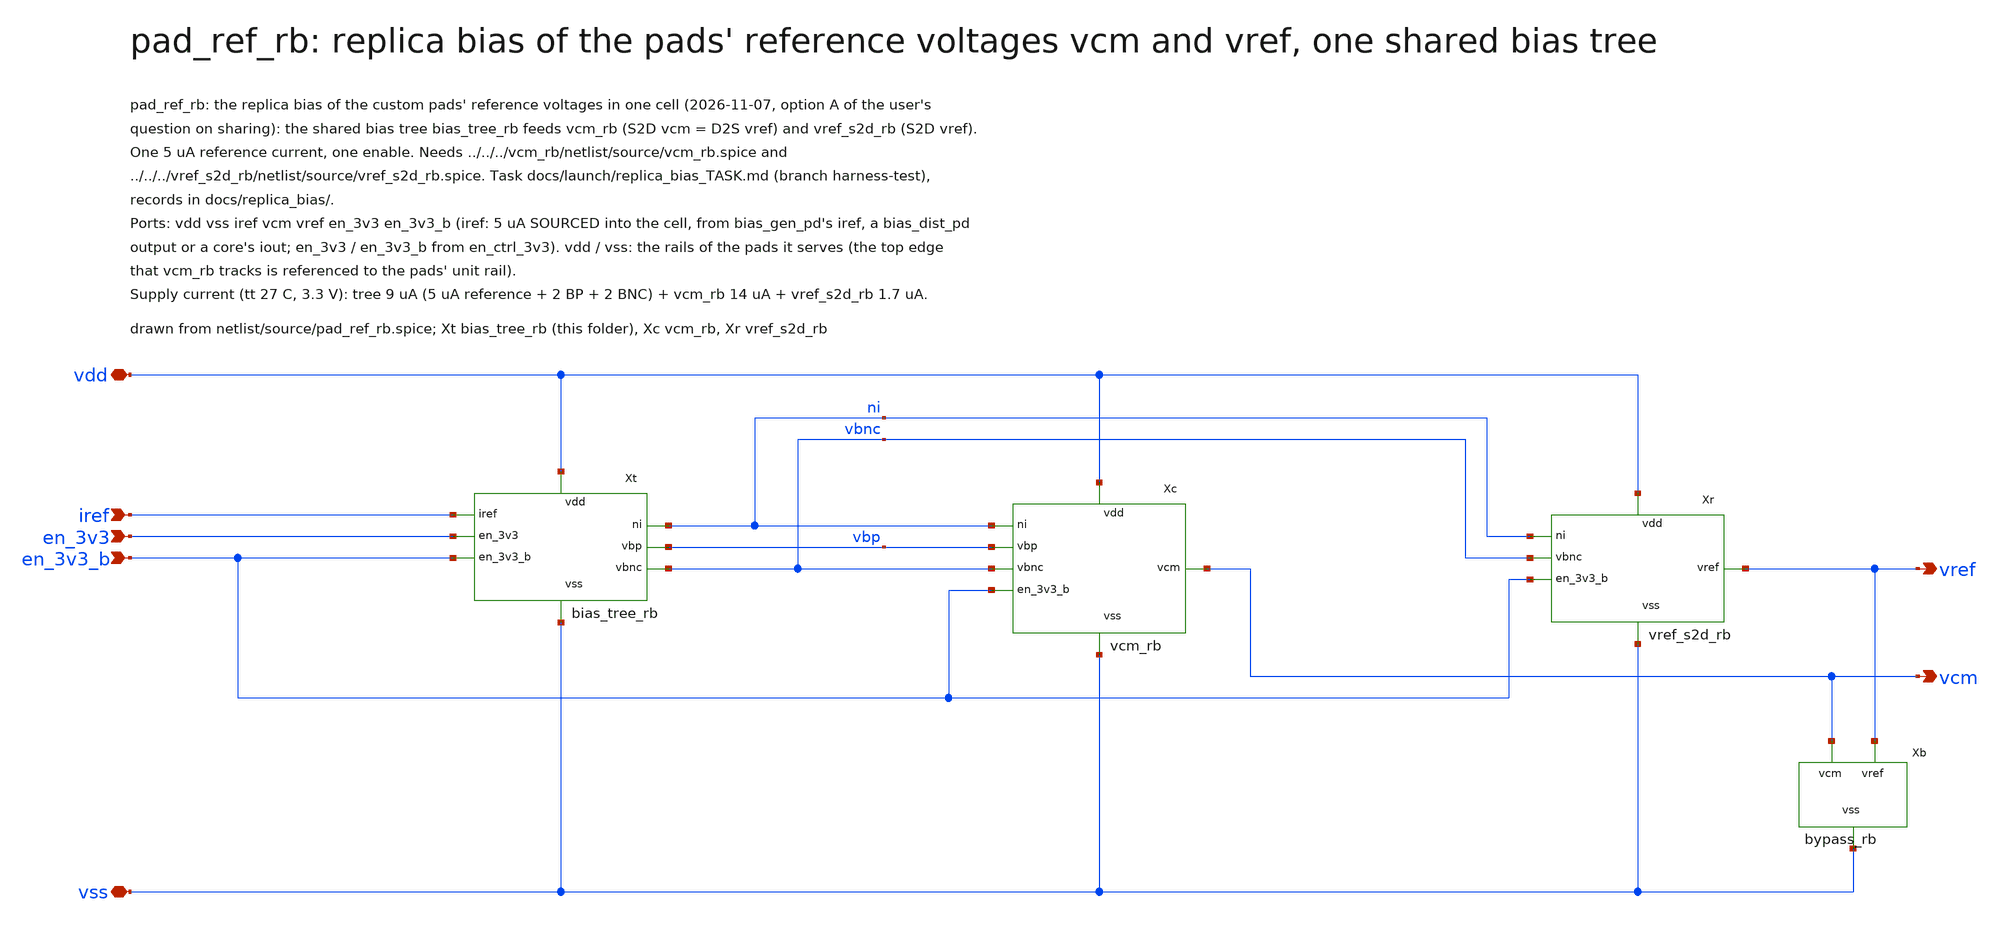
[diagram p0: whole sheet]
** sch_path: macros/pad_ref_rb/schematic/xschem/pad_ref_rb.sch
**.subckt pad_ref_rb vdd vss iref vcm vref en_3v3 en_3v3_b
*.iopin vdd
*.iopin vss
*.ipin iref
*.opin vcm
*.opin vref
*.ipin en_3v3
*.ipin en_3v3_b
Xt vdd vss iref ni vbp vbnc en_3v3 en_3v3_b bias_tree_rb
Xc vdd vss ni vbp vbnc vcm en_3v3_b vcm_rb
Xr vdd vss ni vbnc vref en_3v3_b vref_s2d_rb
Xb vss vcm vref bypass_rb
**.ends

* expanding   symbol:  bias_tree_rb.sym # of pins=8
** sym_path: macros/pad_ref_rb/schematic/xschem/bias_tree_rb.sym
** sch_path: macros/pad_ref_rb/schematic/xschem/bias_tree_rb.sch
.subckt bias_tree_rb vdd vss iref ni vbp vbnc en_3v3 en_3v3_b
*.iopin vdd
*.iopin vss
*.ipin iref
*.opin ni
*.opin vbp
*.opin vbnc
*.ipin en_3v3
*.ipin en_3v3_b
XTGN iref en_3v3 ni vss sg13_hv_nmos w=1u l=0.45u ng=1 m=1 mm_ok=1
XTGP ni en_3v3_b iref vdd sg13_hv_pmos w=1u l=0.45u ng=1 m=1 mm_ok=1
XTDN ni en_3v3_b vss vss sg13_hv_nmos w=1u l=0.45u ng=1 m=1 mm_ok=1
XNI ni ni vss vss sg13_hv_nmos w=6u l=6u ng=1 m=1 mm_ok=1
XNBP vbp ni vss vss sg13_hv_nmos w=2.4u l=6u ng=1 m=1 mm_ok=1
XBP vbp vbp vdd vdd sg13_hv_pmos w=2u l=6u ng=1 m=1 mm_ok=1
XPBNC vbnc vbp vdd vdd sg13_hv_pmos w=2u l=6u ng=1 m=1 mm_ok=1
XBNC vbnc vbnc vss vss sg13_hv_nmos w=1u l=8u ng=1 m=1 mm_ok=1
XMDPBN vdd vbp vdd vdd sg13_hv_pmos w=5u l=6u ng=1 m=1 mm_ok=1
.ends


* expanding   symbol:  vcm_rb.sym # of pins=7
** sym_path: macros/vcm_rb/schematic/xschem/vcm_rb.sym
** sch_path: macros/vcm_rb/schematic/xschem/vcm_rb.sch
.subckt vcm_rb vdd vss ni vbp vbnc vcm en_3v3_b
*.iopin vdd
*.iopin vss
*.ipin ni
*.ipin vbp
*.ipin vbnc
*.opin vcm
*.ipin en_3v3_b
XTR ts vbp vdd vdd sg13_hv_pmos w=5u l=6u ng=1 m=1 mm_ok=1
XMR gh gh ts ts sg13_hv_pmos w=20u l=1u ng=2 m=1 mm_ok=1
XSH1 gh ni vss vss sg13_hv_nmos w=2.4u l=6u ng=1 m=1 mm_ok=1
XSH2 gh ni vss vss sg13_hv_nmos w=2.4u l=6u ng=1 m=1 mm_ok=1
XCY vdd vbnc xp vss sg13_hv_nmos w=15u l=3u ng=1 m=1 mm_ok=1
XSY xp ni vss vss sg13_hv_nmos w=6u l=6u ng=1 m=1 mm_ok=1
XSU m m gh gh sg13_hv_pmos w=1u l=4u ng=1 m=1 mm_ok=1
XSL1 xp xp m m sg13_hv_pmos w=1u l=4u ng=1 m=1 mm_ok=1
XSL2 xp xp m m sg13_hv_pmos w=1u l=4u ng=1 m=1 mm_ok=1
XBT bt vbp vdd vdd sg13_hv_pmos w=5u l=6u ng=1 m=1 mm_ok=1
XBA bd m bt bt sg13_hv_pmos w=20u l=1u ng=2 m=1 mm_ok=1
XBB vcm vcm bt bt sg13_hv_pmos w=20u l=1u ng=2 m=1 mm_ok=1
XBD bd bd vss vss sg13_hv_nmos w=6u l=6u ng=1 m=1 mm_ok=1
XBM vcm bd vss vss sg13_hv_nmos w=6u l=6u ng=1 m=1 mm_ok=1
XCB vss vcm vss vss sg13_hv_nmos w=12u l=12u ng=1 m=1 mm_ok=1
XSPD vcm en_3v3_b vss vss sg13_hv_nmos w=1u l=0.45u ng=1 m=1 mm_ok=1
XMDT[1] vdd vbp vdd vdd sg13_hv_pmos w=5u l=6u ng=1 m=1 mm_ok=1
XMDT[0] vdd vbp vdd vdd sg13_hv_pmos w=5u l=6u ng=1 m=1 mm_ok=1
XMDU[1] vdd vdd vdd vdd sg13_hv_pmos w=20u l=1u ng=2 m=1 mm_ok=1
XMDU[0] vdd vdd vdd vdd sg13_hv_pmos w=20u l=1u ng=2 m=1 mm_ok=1
XMDAU[1] gh m gh gh sg13_hv_pmos w=1u l=4u ng=1 m=1 mm_ok=1
XMDAU[0] gh m gh gh sg13_hv_pmos w=1u l=4u ng=1 m=1 mm_ok=1
XMDAL[1] m xp m m sg13_hv_pmos w=1u l=4u ng=1 m=1 mm_ok=1
XMDAL[0] m xp m m sg13_hv_pmos w=1u l=4u ng=1 m=1 mm_ok=1
XMDM[1] vss bd vss vss sg13_hv_nmos w=2u l=6u ng=1 m=1 mm_ok=1
XMDM[0] vss bd vss vss sg13_hv_nmos w=2u l=6u ng=1 m=1 mm_ok=1
.ends


* expanding   symbol:  vref_s2d_rb.sym # of pins=6
** sym_path: macros/vref_s2d_rb/schematic/xschem/vref_s2d_rb.sym
** sch_path: macros/vref_s2d_rb/schematic/xschem/vref_s2d_rb.sch
.subckt vref_s2d_rb vdd vss ni vbnc vref en_3v3_b
*.iopin vdd
*.iopin vss
*.ipin ni
*.ipin vbnc
*.opin vref
*.ipin en_3v3_b
XF1 vdd vbnc vref vss sg13_hv_nmos w=15u l=3u ng=1 m=1 mm_ok=1
XF2 vdd vbnc vref vss sg13_hv_nmos w=15u l=3u ng=1 m=1 mm_ok=1
XF3 vdd vbnc vref vss sg13_hv_nmos w=15u l=3u ng=1 m=1 mm_ok=1
XF4 vdd vbnc vref vss sg13_hv_nmos w=15u l=3u ng=1 m=1 mm_ok=1
XSF vref ni vss vss sg13_hv_nmos w=2u l=6u ng=1 m=1 mm_ok=1
XCB1 vss vref vss vss sg13_hv_nmos w=12u l=12u ng=1 m=1 mm_ok=1
XCB2 vss vref vss vss sg13_hv_nmos w=12u l=12u ng=1 m=1 mm_ok=1
XSPD vref en_3v3_b vss vss sg13_hv_nmos w=1u l=0.45u ng=1 m=1 mm_ok=1
.ends


* expanding   symbol:  bypass_rb.sym # of pins=3
** sym_path: macros/pad_ref_rb/schematic/xschem/bypass_rb.sym
** sch_path: macros/pad_ref_rb/schematic/xschem/bypass_rb.sch
.subckt bypass_rb vss vcm vref
*.iopin vss
*.iopin vcm
*.iopin vref
XCBM vss vcm vss vss sg13_hv_nmos w=12u l=12u ng=1 m={ncm} mm_ok=1
XCBR vss vref vss vss sg13_hv_nmos w=12u l=12u ng=1 m={ncr} mm_ok=1
.ends

.end
